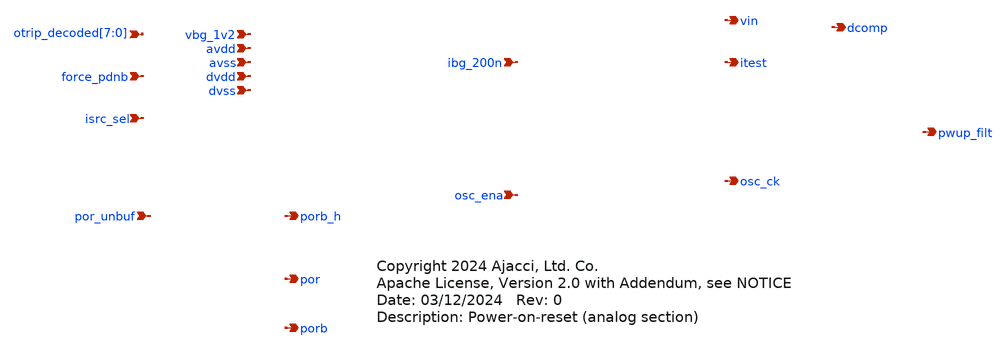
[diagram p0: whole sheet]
** sch_path: xschem/por_ana_rcx.sch
* Copyright 2024 Ajacci, Ltd. Co.
* Apache License, Version 2.0 with Addendum, see NOTICE
**.subckt por_ana_rcx vbg_1v2 avdd avss dvdd dvss force_pdnb isrc_sel ibg_200n pwup_filt itest
*+ osc_ena osc_ck
*+ otrip_decoded[7],otrip_decoded[6],otrip_decoded[5],otrip_decoded[4],otrip_decoded[3],otrip_decoded[2],otrip_decoded[1],otrip_decoded[0] vin por_unbuf porb_h por porb dcomp
*.ipin vbg_1v2
*.ipin avdd
*.ipin avss
*.ipin dvdd
*.ipin dvss
*.ipin force_pdnb
*.ipin isrc_sel
*.ipin ibg_200n
*.opin pwup_filt
*.opin itest
*.ipin osc_ena
*.opin osc_ck
*.ipin
*+ otrip_decoded[7],otrip_decoded[6],otrip_decoded[5],otrip_decoded[4],otrip_decoded[3],otrip_decoded[2],otrip_decoded[1],otrip_decoded[0]
*.opin vin
*.ipin por_unbuf
*.opin porb_h
*.opin por
*.opin porb
*.opin dcomp
**** begin user architecture code



.include mag/rcx/por_ana_rcx.spice

xIana vin otrip_decoded[7] otrip_decoded[6] otrip_decoded[5] otrip_decoded[4]  otrip_decoded[3]
+ otrip_decoded[2] otrip_decoded[1] otrip_decoded[0] vbg_1v2 avdd itest avss ibg_200n force_pdnb dvdd dvss dcomp
+ isrc_sel pwup_filt osc_ck osc_ena porb_h por_unbuf por porb por_ana



**** end user architecture code
**.ends
.end
